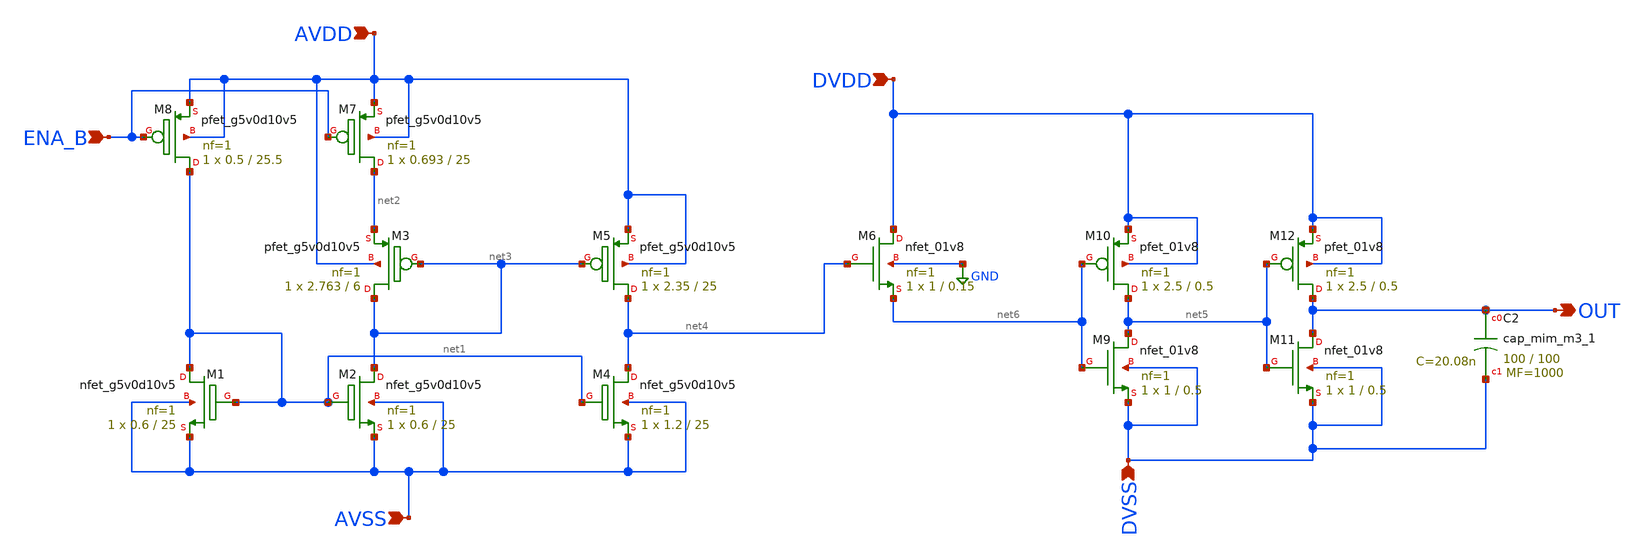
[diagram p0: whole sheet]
** sch_path: xschem/sky130_dok_ip_brown_out_detector.sch
**.subckt sky130_dok_ip_brown_out_detector AVDD DVDD AVSS DVSS ENA_B OUT
*.ipin AVDD
*.ipin DVDD
*.ipin AVSS
*.ipin DVSS
*.ipin ENA_B
*.opin OUT
XM1 net1 net1 AVSS AVSS sky130_fd_pr__nfet_g5v0d10v5 L=25 W=0.6 nf=1 ad='int((nf+1)/2) * W/nf * 0.29'
+ as='int((nf+2)/2) * W/nf * 0.29' pd='2*int((nf+1)/2) * (W/nf + 0.29)' ps='2*int((nf+2)/2) * (W/nf + 0.29)'
+ nrd='0.29 / W' nrs='0.29 / W' sa=0 sb=0 sd=0 mult=1 m=1
XM2 net3 net1 AVSS AVSS sky130_fd_pr__nfet_g5v0d10v5 L=25 W=0.6 nf=1 ad='int((nf+1)/2) * W/nf * 0.29'
+ as='int((nf+2)/2) * W/nf * 0.29' pd='2*int((nf+1)/2) * (W/nf + 0.29)' ps='2*int((nf+2)/2) * (W/nf + 0.29)'
+ nrd='0.29 / W' nrs='0.29 / W' sa=0 sb=0 sd=0 mult=1 m=1
XM4 net4 net1 AVSS AVSS sky130_fd_pr__nfet_g5v0d10v5 L=25 W=1.2 nf=1 ad='int((nf+1)/2) * W/nf * 0.29'
+ as='int((nf+2)/2) * W/nf * 0.29' pd='2*int((nf+1)/2) * (W/nf + 0.29)' ps='2*int((nf+2)/2) * (W/nf + 0.29)'
+ nrd='0.29 / W' nrs='0.29 / W' sa=0 sb=0 sd=0 mult=1 m=1
XM5 net4 net3 AVDD AVDD sky130_fd_pr__pfet_g5v0d10v5 L=25 W=2.35 nf=1 ad='int((nf+1)/2) * W/nf * 0.29'
+ as='int((nf+2)/2) * W/nf * 0.29' pd='2*int((nf+1)/2) * (W/nf + 0.29)' ps='2*int((nf+2)/2) * (W/nf + 0.29)'
+ nrd='0.29 / W' nrs='0.29 / W' sa=0 sb=0 sd=0 mult=1 m=1
XM3 net3 net3 net2 AVDD sky130_fd_pr__pfet_g5v0d10v5 L=6 W=2.763 nf=1 ad='int((nf+1)/2) * W/nf * 0.29'
+ as='int((nf+2)/2) * W/nf * 0.29' pd='2*int((nf+1)/2) * (W/nf + 0.29)' ps='2*int((nf+2)/2) * (W/nf + 0.29)'
+ nrd='0.29 / W' nrs='0.29 / W' sa=0 sb=0 sd=0 mult=1 m=1
XM7 net2 ENA_B AVDD AVDD sky130_fd_pr__pfet_g5v0d10v5 L=25 W=0.693 nf=1 ad='int((nf+1)/2) * W/nf * 0.29'
+ as='int((nf+2)/2) * W/nf * 0.29' pd='2*int((nf+1)/2) * (W/nf + 0.29)' ps='2*int((nf+2)/2) * (W/nf + 0.29)'
+ nrd='0.29 / W' nrs='0.29 / W' sa=0 sb=0 sd=0 mult=1 m=1
XM8 net1 ENA_B AVDD AVDD sky130_fd_pr__pfet_g5v0d10v5 L=25.5 W=0.5 nf=1 ad='int((nf+1)/2) * W/nf * 0.29'
+ as='int((nf+2)/2) * W/nf * 0.29' pd='2*int((nf+1)/2) * (W/nf + 0.29)' ps='2*int((nf+2)/2) * (W/nf + 0.29)'
+ nrd='0.29 / W' nrs='0.29 / W' sa=0 sb=0 sd=0 mult=1 m=1
XM6 DVDD net4 net6 GND sky130_fd_pr__nfet_01v8 L=0.15 W=1 nf=1 ad='int((nf+1)/2) * W/nf * 0.29' as='int((nf+2)/2) * W/nf * 0.29'
+ pd='2*int((nf+1)/2) * (W/nf + 0.29)' ps='2*int((nf+2)/2) * (W/nf + 0.29)' nrd='0.29 / W' nrs='0.29 / W'
+ sa=0 sb=0 sd=0 mult=1 m=1
XM9 net5 net6 DVSS DVSS sky130_fd_pr__nfet_01v8 L=0.5 W=1 nf=1 ad='int((nf+1)/2) * W/nf * 0.29' as='int((nf+2)/2) * W/nf * 0.29'
+ pd='2*int((nf+1)/2) * (W/nf + 0.29)' ps='2*int((nf+2)/2) * (W/nf + 0.29)' nrd='0.29 / W' nrs='0.29 / W'
+ sa=0 sb=0 sd=0 mult=1 m=1
XM10 net5 net6 DVDD DVDD sky130_fd_pr__pfet_01v8 L=0.5 W=2.5 nf=1 ad='int((nf+1)/2) * W/nf * 0.29' as='int((nf+2)/2) * W/nf * 0.29'
+ pd='2*int((nf+1)/2) * (W/nf + 0.29)' ps='2*int((nf+2)/2) * (W/nf + 0.29)' nrd='0.29 / W' nrs='0.29 / W'
+ sa=0 sb=0 sd=0 mult=1 m=1
XM11 OUT net5 DVSS DVSS sky130_fd_pr__nfet_01v8 L=0.5 W=1 nf=1 ad='int((nf+1)/2) * W/nf * 0.29' as='int((nf+2)/2) * W/nf * 0.29'
+ pd='2*int((nf+1)/2) * (W/nf + 0.29)' ps='2*int((nf+2)/2) * (W/nf + 0.29)' nrd='0.29 / W' nrs='0.29 / W'
+ sa=0 sb=0 sd=0 mult=1 m=1
XM12 OUT net5 DVDD DVDD sky130_fd_pr__pfet_01v8 L=0.5 W=2.5 nf=1 ad='int((nf+1)/2) * W/nf * 0.29' as='int((nf+2)/2) * W/nf * 0.29'
+ pd='2*int((nf+1)/2) * (W/nf + 0.29)' ps='2*int((nf+2)/2) * (W/nf + 0.29)' nrd='0.29 / W' nrs='0.29 / W'
+ sa=0 sb=0 sd=0 mult=1 m=1
XC2 OUT DVSS sky130_fd_pr__cap_mim_m3_1 W=100 L=100 MF=1000 m=1000
**.ends
.GLOBAL GND
.end
